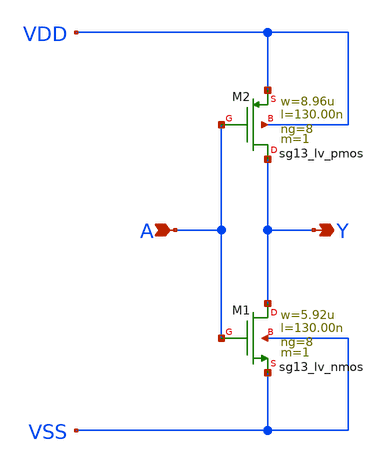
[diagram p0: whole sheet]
** sch_path: ihp-sg13g2/libs.ref/sg13g2_stdcell/sch/xschem/sg13g2_inv_8.sch
* Copyright 2023 IHP PDK Authors
* Licensed under the Apache License, Version 2.0 (the "License");
* you may not use this file except in compliance with the License.
* You may obtain a copy of the License at
* https://www.apache.org/licenses/LICENSE-2.0
* Unless required by applicable law or agreed to in writing, software
* distributed under the License is distributed on an "AS IS" BASIS,
* WITHOUT WARRANTIES OR CONDITIONS OF ANY KIND, either express or implied.
* See the License for the specific language governing permissions and
* limitations under the License.
**.subckt sg13g2_inv_8 Y A
*.opin Y
*.ipin A
XM1 Y A VSS VSS sg13_lv_nmos w=5.92u l=130.00n ng=8 m=1 mm_ok=1
XM2 Y A VDD VDD sg13_lv_pmos w=8.96u l=130.00n ng=8 m=1 mm_ok=1
**.ends
.end
